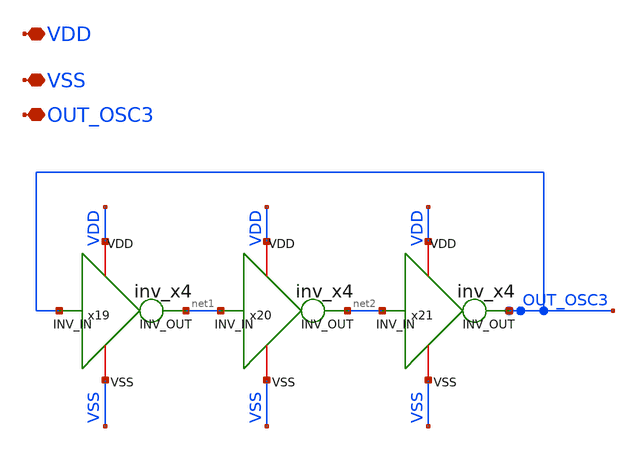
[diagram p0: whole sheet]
** sch_path: xschem/OSC3.sch
**.subckt OSC3 VDD VSS OUT_OSC3
*.iopin VDD
*.iopin VSS
*.iopin OUT_OSC3
x19 VDD VSS net1 OUT_OSC3 inv_x4
x20 VDD VSS net2 net1 inv_x4
x21 VDD VSS OUT_OSC3 net2 inv_x4
**.ends

* expanding   symbol:  inv_x4.sym # of pins=4
** sym_path: xschem/inv_x4.sym
** sch_path: xschem/inv_x4.sch
.subckt inv_x4 VDD VSS INV_OUT INV_IN
*.ipin INV_IN
*.opin INV_OUT
*.iopin VDD
*.iopin VSS
XM3 INV_OUT INV_IN VDD VDD sky130_fd_pr__pfet_01v8 L=10 W=2 nf=1 ad='int((nf+1)/2) * W/nf * 0.29' as='int((nf+2)/2) * W/nf * 0.29'
+ pd='2*int((nf+1)/2) * (W/nf + 0.29)' ps='2*int((nf+2)/2) * (W/nf + 0.29)' nrd='0.29 / W' nrs='0.29 / W'
+ sa=0 sb=0 sd=0 mult=1 m=1
XM5 INV_OUT INV_IN VSS VSS sky130_fd_pr__nfet_01v8 L=10 W=1 nf=1 ad='int((nf+1)/2) * W/nf * 0.29' as='int((nf+2)/2) * W/nf * 0.29'
+ pd='2*int((nf+1)/2) * (W/nf + 0.29)' ps='2*int((nf+2)/2) * (W/nf + 0.29)' nrd='0.29 / W' nrs='0.29 / W'
+ sa=0 sb=0 sd=0 mult=1 m=1
.ends

.end
